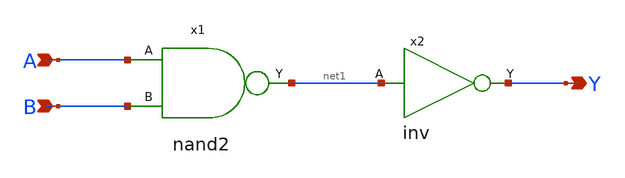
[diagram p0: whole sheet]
** sch_path: circuits/xschem/and.sch
**.subckt and A Y B
*.ipin A
*.opin Y
*.ipin B
x1 A net1 B nand2
x2 net1 Y inv
**.ends

* expanding   symbol:  /home/ksnarr/magic/library/xschem/nand2.sym # of pins=3
** sym_path: library/xschem/nand2.sym
** sch_path: library/xschem/nand2.sch
.subckt nand2 A Y B
*.opin Y
*.ipin A
*.ipin B
XM1 Y B net1 GND sky130_fd_pr__nfet_01v8 L=0.15 W=1 nf=1 ad='int((nf+1)/2) * W/nf * 0.29' as='int((nf+2)/2) * W/nf * 0.29'
+ pd='2*int((nf+1)/2) * (W/nf + 0.29)' ps='2*int((nf+2)/2) * (W/nf + 0.29)' nrd='0.29 / W' nrs='0.29 / W'
+ sa=0 sb=0 sd=0 mult=1 m=1
XM2 Y B VDD VDD sky130_fd_pr__pfet_01v8 L=0.15 W=1 nf=1 ad='int((nf+1)/2) * W/nf * 0.29' as='int((nf+2)/2) * W/nf * 0.29'
+ pd='2*int((nf+1)/2) * (W/nf + 0.29)' ps='2*int((nf+2)/2) * (W/nf + 0.29)' nrd='0.29 / W' nrs='0.29 / W'
+ sa=0 sb=0 sd=0 mult=1 m=1
XM3 Y A VDD VDD sky130_fd_pr__pfet_01v8 L=0.15 W=1 nf=1 ad='int((nf+1)/2) * W/nf * 0.29' as='int((nf+2)/2) * W/nf * 0.29'
+ pd='2*int((nf+1)/2) * (W/nf + 0.29)' ps='2*int((nf+2)/2) * (W/nf + 0.29)' nrd='0.29 / W' nrs='0.29 / W'
+ sa=0 sb=0 sd=0 mult=1 m=1
XM4 net1 A GND GND sky130_fd_pr__nfet_01v8 L=0.15 W=1 nf=1 ad='int((nf+1)/2) * W/nf * 0.29' as='int((nf+2)/2) * W/nf * 0.29'
+ pd='2*int((nf+1)/2) * (W/nf + 0.29)' ps='2*int((nf+2)/2) * (W/nf + 0.29)' nrd='0.29 / W' nrs='0.29 / W'
+ sa=0 sb=0 sd=0 mult=1 m=1
.ends


* expanding   symbol:  /home/ksnarr/magic/library/xschem/inv.sym # of pins=2
** sym_path: library/xschem/inv.sym
** sch_path: library/xschem/inv.sch
.subckt inv A Y
*.opin Y
*.ipin A
XM1 Y A GND GND sky130_fd_pr__nfet_01v8 L=0.15 W=1 nf=1 ad='int((nf+1)/2) * W/nf * 0.29' as='int((nf+2)/2) * W/nf * 0.29'
+ pd='2*int((nf+1)/2) * (W/nf + 0.29)' ps='2*int((nf+2)/2) * (W/nf + 0.29)' nrd='0.29 / W' nrs='0.29 / W'
+ sa=0 sb=0 sd=0 mult=1 m=1
XM2 Y A VDD VDD sky130_fd_pr__pfet_01v8 L=0.15 W=1 nf=1 ad='int((nf+1)/2) * W/nf * 0.29' as='int((nf+2)/2) * W/nf * 0.29'
+ pd='2*int((nf+1)/2) * (W/nf + 0.29)' ps='2*int((nf+2)/2) * (W/nf + 0.29)' nrd='0.29 / W' nrs='0.29 / W'
+ sa=0 sb=0 sd=0 mult=1 m=1
.ends

.GLOBAL VDD
.GLOBAL GND
.end
